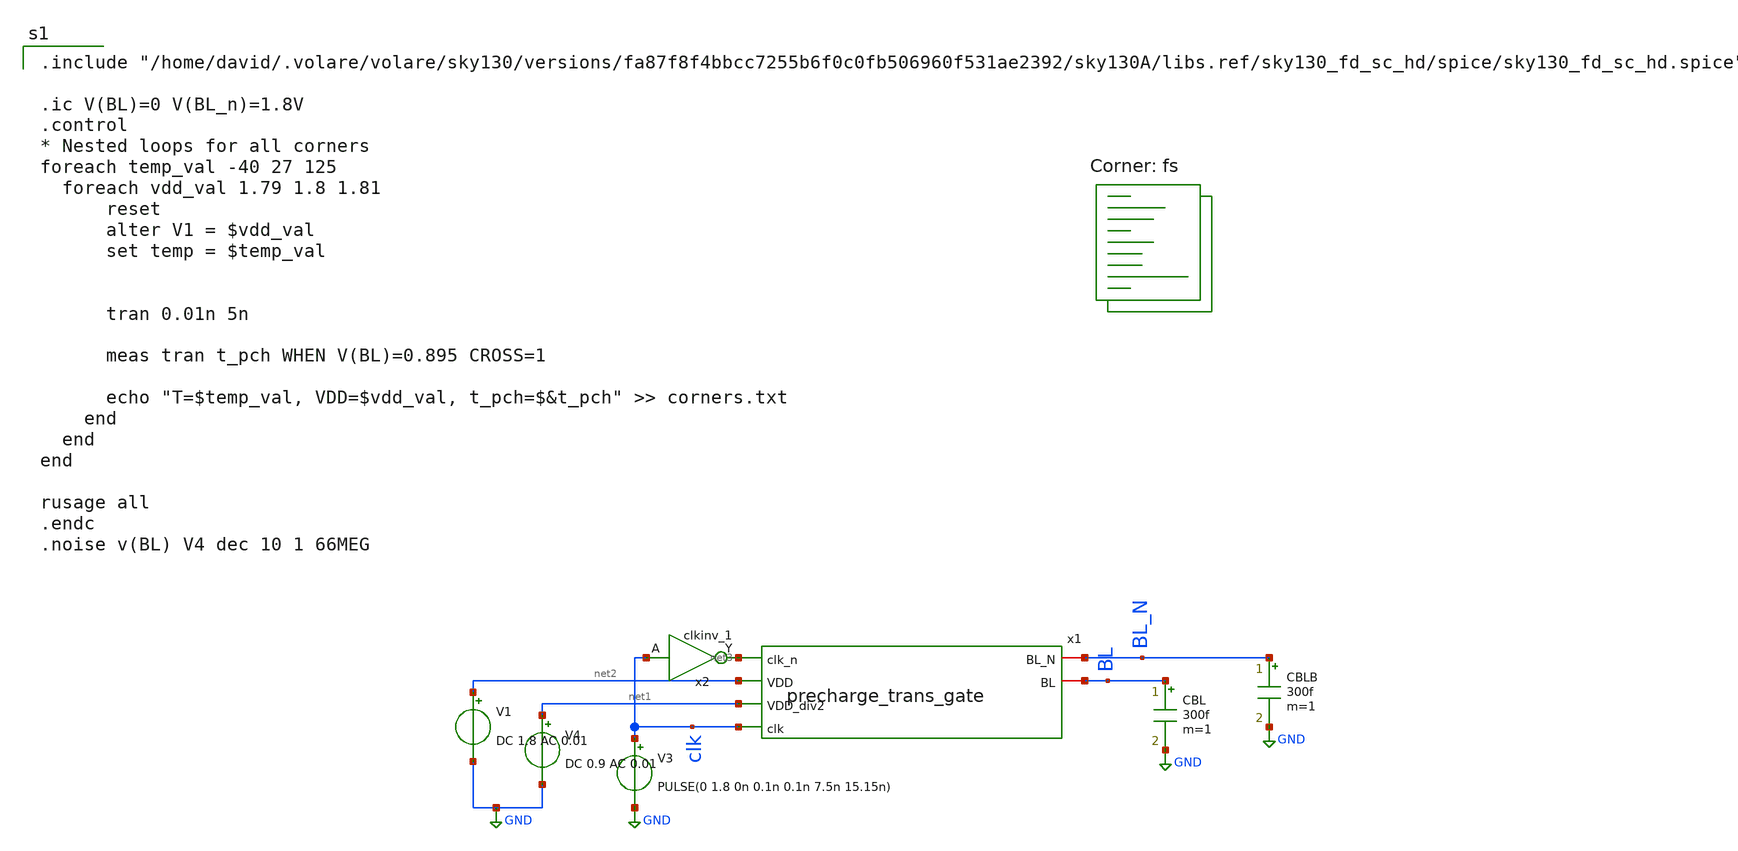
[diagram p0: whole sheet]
** sch_path: analog/schematics/trans_gate_tb.sch
**.subckt trans_gate_tb
V3 clk GND PULSE(0 1.8 0n 0.1n 0.1n 7.5n 15.15n)
x2 clk VGND VNB VPB VPWR net3 sky130_fd_sc_hd__clkinv_1
V4 net1 GND DC 0.9 AC 0.01
CBLB BL_N GND 300f m=1
CBL BL GND 300f m=1
x1 net3 BL_N BL net2 net1 clk precharge_trans_gate
V1 net2 GND DC 1.8 AC 0.01
**** begin user architecture code

.include "/home/david/.volare/volare/sky130/versions/fa87f8f4bbcc7255b6f0c0fb506960f531ae2392/sky130A/libs.ref/sky130_fd_sc_hd/spice/sky130_fd_sc_hd.spice"

.ic V(BL)=0 V(BL_n)=1.8V
.control
* Nested loops for all corners
foreach temp_val -40 27 125
  foreach vdd_val 1.79 1.8 1.81
      reset
      alter V1 = $vdd_val
      set temp = $temp_val


      tran 0.01n 5n

      meas tran t_pch WHEN V(BL)=0.895 CROSS=1

      echo "T=$temp_val, VDD=$vdd_val, t_pch=$&t_pch" >> corners.txt
    end
  end
end

rusage all
.endc
.noise v(BL) V4 dec 10 1 66MEG

.lib $::SKYWATER_MODELS/sky130.lib.spice fs
**** end user architecture code
**.ends
.GLOBAL GND
.end
